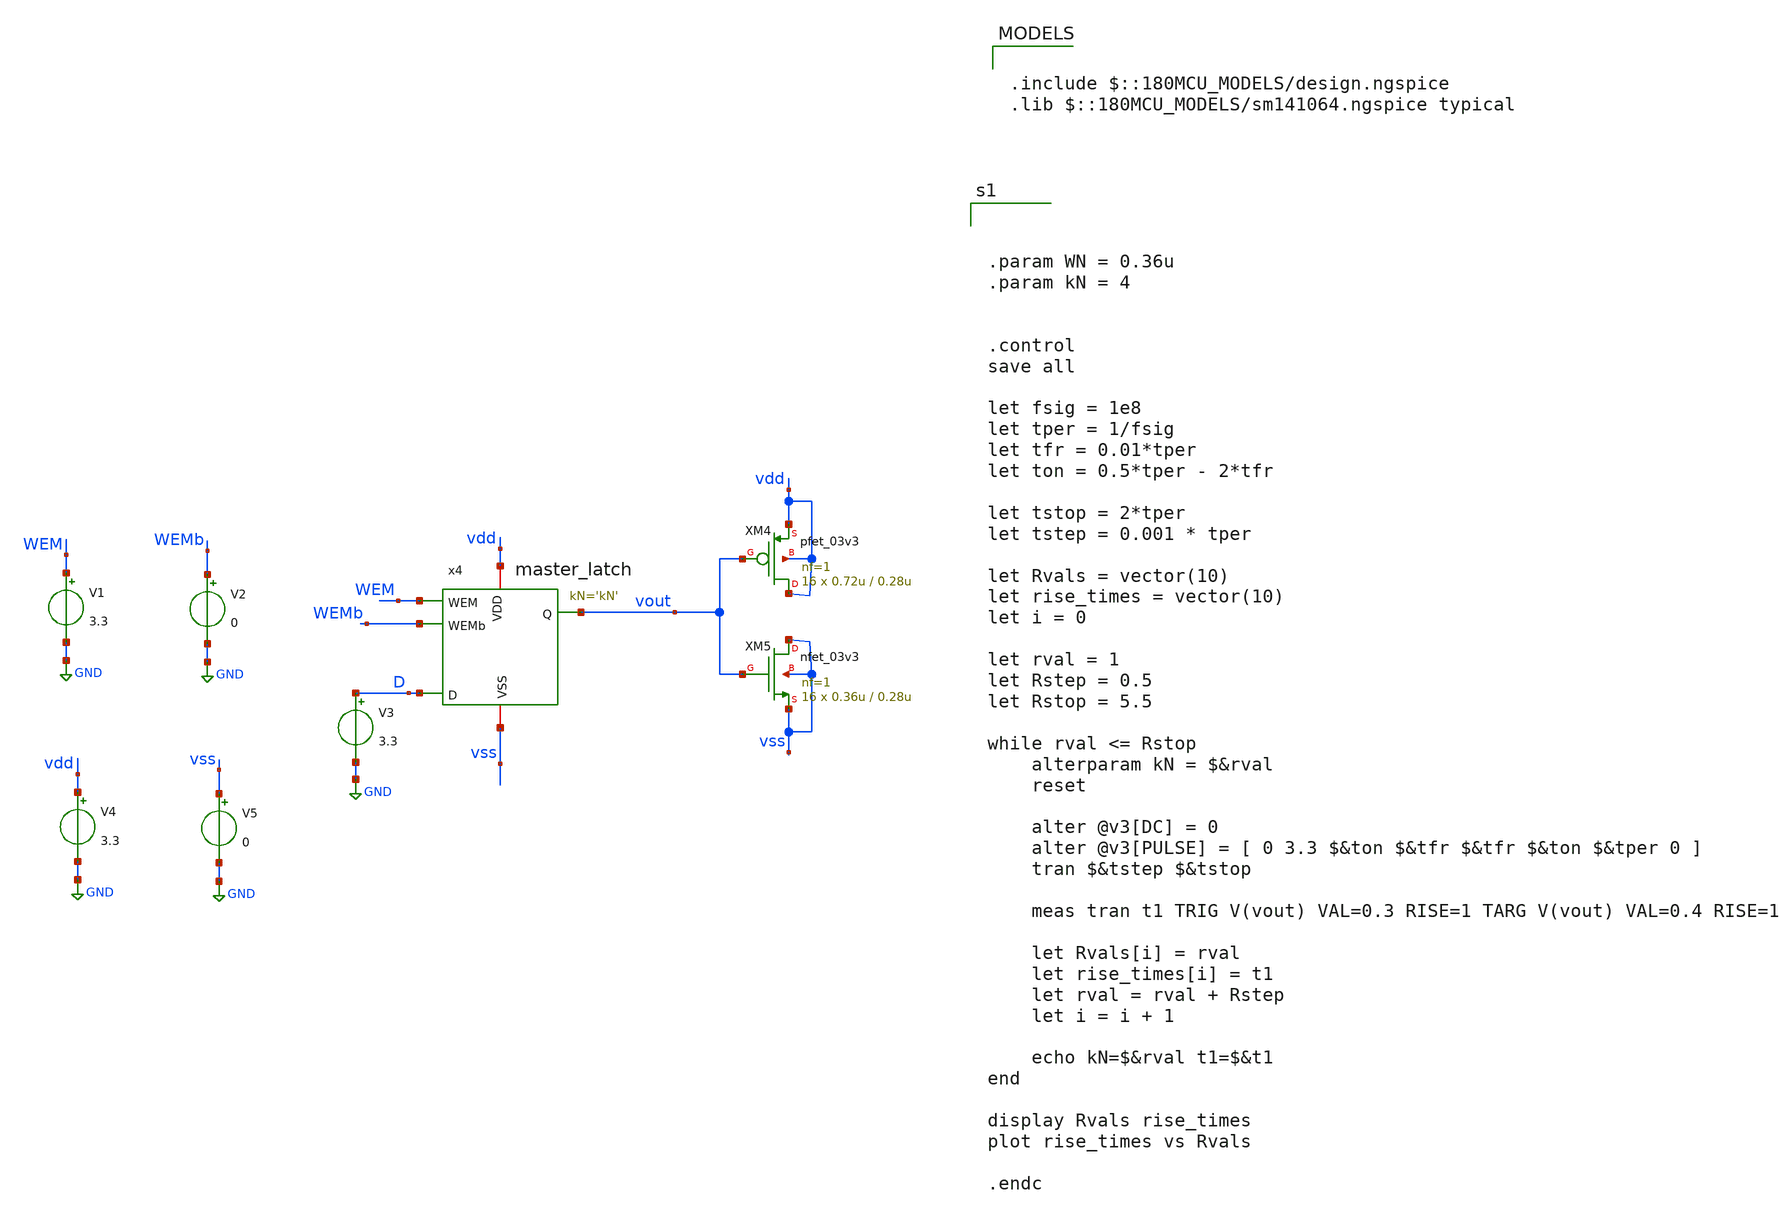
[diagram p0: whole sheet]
** sch_path: CAD3/sizing_tb_martin.sch
**.subckt sizing_tb_martin
x4 vdd vss vout WEM WEMb D master_latch kN='kN'
XM4 vdd vout vdd vdd pfet_03v3 L=0.28u W=0.72u nf=1 ad='int((nf+1)/2) * W/nf * 0.18u' as='int((nf+2)/2) * W/nf * 0.18u'
+ pd='2*int((nf+1)/2) * (W/nf + 0.18u)' ps='2*int((nf+2)/2) * (W/nf + 0.18u)' nrd='0.18u / W' nrs='0.18u / W'
+ sa=0 sb=0 sd=0 m=16
XM5 vss vout vss vss nfet_03v3 L=0.28u W=0.36u nf=1 ad='int((nf+1)/2) * W/nf * 0.18u' as='int((nf+2)/2) * W/nf * 0.18u'
+ pd='2*int((nf+1)/2) * (W/nf + 0.18u)' ps='2*int((nf+2)/2) * (W/nf + 0.18u)' nrd='0.18u / W' nrs='0.18u / W'
+ sa=0 sb=0 sd=0 m=16
V1 WEM GND 3.3
V3 D GND 3.3
V2 WEMb GND 0
V4 vdd GND 3.3
V5 vss GND 0
**** begin user architecture code

.include $::180MCU_MODELS/design.ngspice
.lib $::180MCU_MODELS/sm141064.ngspice typical




.param WN = 0.36u
.param kN = 4


.control
save all

let fsig = 1e8
let tper = 1/fsig
let tfr = 0.01*tper
let ton = 0.5*tper - 2*tfr

let tstop = 2*tper
let tstep = 0.001 * tper

let Rvals = vector(10)
let rise_times = vector(10)
let i = 0

let rval = 1
let Rstep = 0.5
let Rstop = 5.5

while rval <= Rstop
	alterparam kN = $&rval
	reset

	alter @v3[DC] = 0
	alter @v3[PULSE] = [ 0 3.3 $&ton $&tfr $&tfr $&ton $&tper 0 ]
	tran $&tstep $&tstop

	meas tran t1 TRIG V(vout) VAL=0.3 RISE=1 TARG V(vout) VAL=0.4 RISE=1

	let Rvals[i] = rval
	let rise_times[i] = t1
	let rval = rval + Rstep
	let i = i + 1

	echo kN=$&rval t1=$&t1
end

display Rvals rise_times
plot rise_times vs Rvals

.endc



**** end user architecture code
**.ends

* expanding   symbol:  engn1600-team1/CAD3/master_latch.sym # of pins=6
** sym_path: CAD3/master_latch.sym
** sch_path: CAD3/master_latch.sch
.subckt master_latch VDD VSS Q WEM WEMb D  kN=1
*.ipin D
*.ipin WEMb
*.ipin WEM
*.iopin VSS
*.iopin VDD
*.opin Q
XM3 net1 WEMb net2 VDD pfet_03v3 L=0.28u W=0.36u nf=1 ad='int((nf+1)/2) * W/nf * 0.18u' as='int((nf+2)/2) * W/nf * 0.18u'
+ pd='2*int((nf+1)/2) * (W/nf + 0.18u)' ps='2*int((nf+2)/2) * (W/nf + 0.18u)' nrd='0.18u / W' nrs='0.18u / W'
+ sa=0 sb=0 sd=0 m=1
XM7 net1 D VDD VDD pfet_03v3 L=0.28u W=0.72u nf=1 ad='int((nf+1)/2) * W/nf * 0.18u' as='int((nf+2)/2) * W/nf * 0.18u'
+ pd='2*int((nf+1)/2) * (W/nf + 0.18u)' ps='2*int((nf+2)/2) * (W/nf + 0.18u)' nrd='0.18u / W' nrs='0.18u / W'
+ sa=0 sb=0 sd=0 m=1
XM8 Q net2 VDD VDD pfet_03v3 L=0.28u W=0.72u nf=4 ad='int((nf+1)/2) * W/nf * 0.18u' as='int((nf+2)/2) * W/nf * 0.18u'
+ pd='2*int((nf+1)/2) * (W/nf + 0.18u)' ps='2*int((nf+2)/2) * (W/nf + 0.18u)' nrd='0.18u / W' nrs='0.18u / W'
+ sa=0 sb=0 sd=0 m=1
XM9 net3 net2 VDD VDD pfet_03v3 L=0.28u W=0.36u nf=1 ad='int((nf+1)/2) * W/nf * 0.18u' as='int((nf+2)/2) * W/nf * 0.18u'
+ pd='2*int((nf+1)/2) * (W/nf + 0.18u)' ps='2*int((nf+2)/2) * (W/nf + 0.18u)' nrd='0.18u / W' nrs='0.18u / W'
+ sa=0 sb=0 sd=0 m=1
XM10 VDD WEM net5 VDD pfet_03v3 L=0.28u W=0.36u nf=1 ad='int((nf+1)/2) * W/nf * 0.18u' as='int((nf+2)/2) * W/nf * 0.18u'
+ pd='2*int((nf+1)/2) * (W/nf + 0.18u)' ps='2*int((nf+2)/2) * (W/nf + 0.18u)' nrd='0.18u / W' nrs='0.18u / W'
+ sa=0 sb=0 sd=0 m=1
XM12 net5 net3 net2 VDD pfet_03v3 L=0.28u W=0.36u nf=1 ad='int((nf+1)/2) * W/nf * 0.18u' as='int((nf+2)/2) * W/nf * 0.18u'
+ pd='2*int((nf+1)/2) * (W/nf + 0.18u)' ps='2*int((nf+2)/2) * (W/nf + 0.18u)' nrd='0.18u / W' nrs='0.18u / W'
+ sa=0 sb=0 sd=0 m=1
XM19 net1 D VSS VSS nfet_03v3 L=0.28u W=0.36u nf=1 ad='int((nf+1)/2) * W/nf * 0.18u' as='int((nf+2)/2) * W/nf * 0.18u'
+ pd='2*int((nf+1)/2) * (W/nf + 0.18u)' ps='2*int((nf+2)/2) * (W/nf + 0.18u)' nrd='0.18u / W' nrs='0.18u / W'
+ sa=0 sb=0 sd=0 m=1
XM20 net1 WEM net2 VSS nfet_03v3 L=0.28u W=0.36u nf=1 ad='int((nf+1)/2) * W/nf * 0.18u' as='int((nf+2)/2) * W/nf * 0.18u'
+ pd='2*int((nf+1)/2) * (W/nf + 0.18u)' ps='2*int((nf+2)/2) * (W/nf + 0.18u)' nrd='0.18u / W' nrs='0.18u / W'
+ sa=0 sb=0 sd=0 m=1
XM21 Q net2 VSS VSS nfet_03v3 L=0.28u W=0.36u nf=4 ad='int((nf+1)/2) * W/nf * 0.18u' as='int((nf+2)/2) * W/nf * 0.18u'
+ pd='2*int((nf+1)/2) * (W/nf + 0.18u)' ps='2*int((nf+2)/2) * (W/nf + 0.18u)' nrd='0.18u / W' nrs='0.18u / W'
+ sa=0 sb=0 sd=0 m=1
XM22 net3 net2 VSS VSS nfet_03v3 L=0.28u W=0.36u nf=1 ad='int((nf+1)/2) * W/nf * 0.18u' as='int((nf+2)/2) * W/nf * 0.18u'
+ pd='2*int((nf+1)/2) * (W/nf + 0.18u)' ps='2*int((nf+2)/2) * (W/nf + 0.18u)' nrd='0.18u / W' nrs='0.18u / W'
+ sa=0 sb=0 sd=0 m=1
XM23 net4 net3 net2 VSS nfet_03v3 L=0.28u W=0.36u nf=1 ad='int((nf+1)/2) * W/nf * 0.18u' as='int((nf+2)/2) * W/nf * 0.18u'
+ pd='2*int((nf+1)/2) * (W/nf + 0.18u)' ps='2*int((nf+2)/2) * (W/nf + 0.18u)' nrd='0.18u / W' nrs='0.18u / W'
+ sa=0 sb=0 sd=0 m=1
XM24 VSS WEMb net4 VSS nfet_03v3 L=0.28u W=0.36u nf=1 ad='int((nf+1)/2) * W/nf * 0.18u' as='int((nf+2)/2) * W/nf * 0.18u'
+ pd='2*int((nf+1)/2) * (W/nf + 0.18u)' ps='2*int((nf+2)/2) * (W/nf + 0.18u)' nrd='0.18u / W' nrs='0.18u / W'
+ sa=0 sb=0 sd=0 m=1
.ends

.GLOBAL GND
.end
